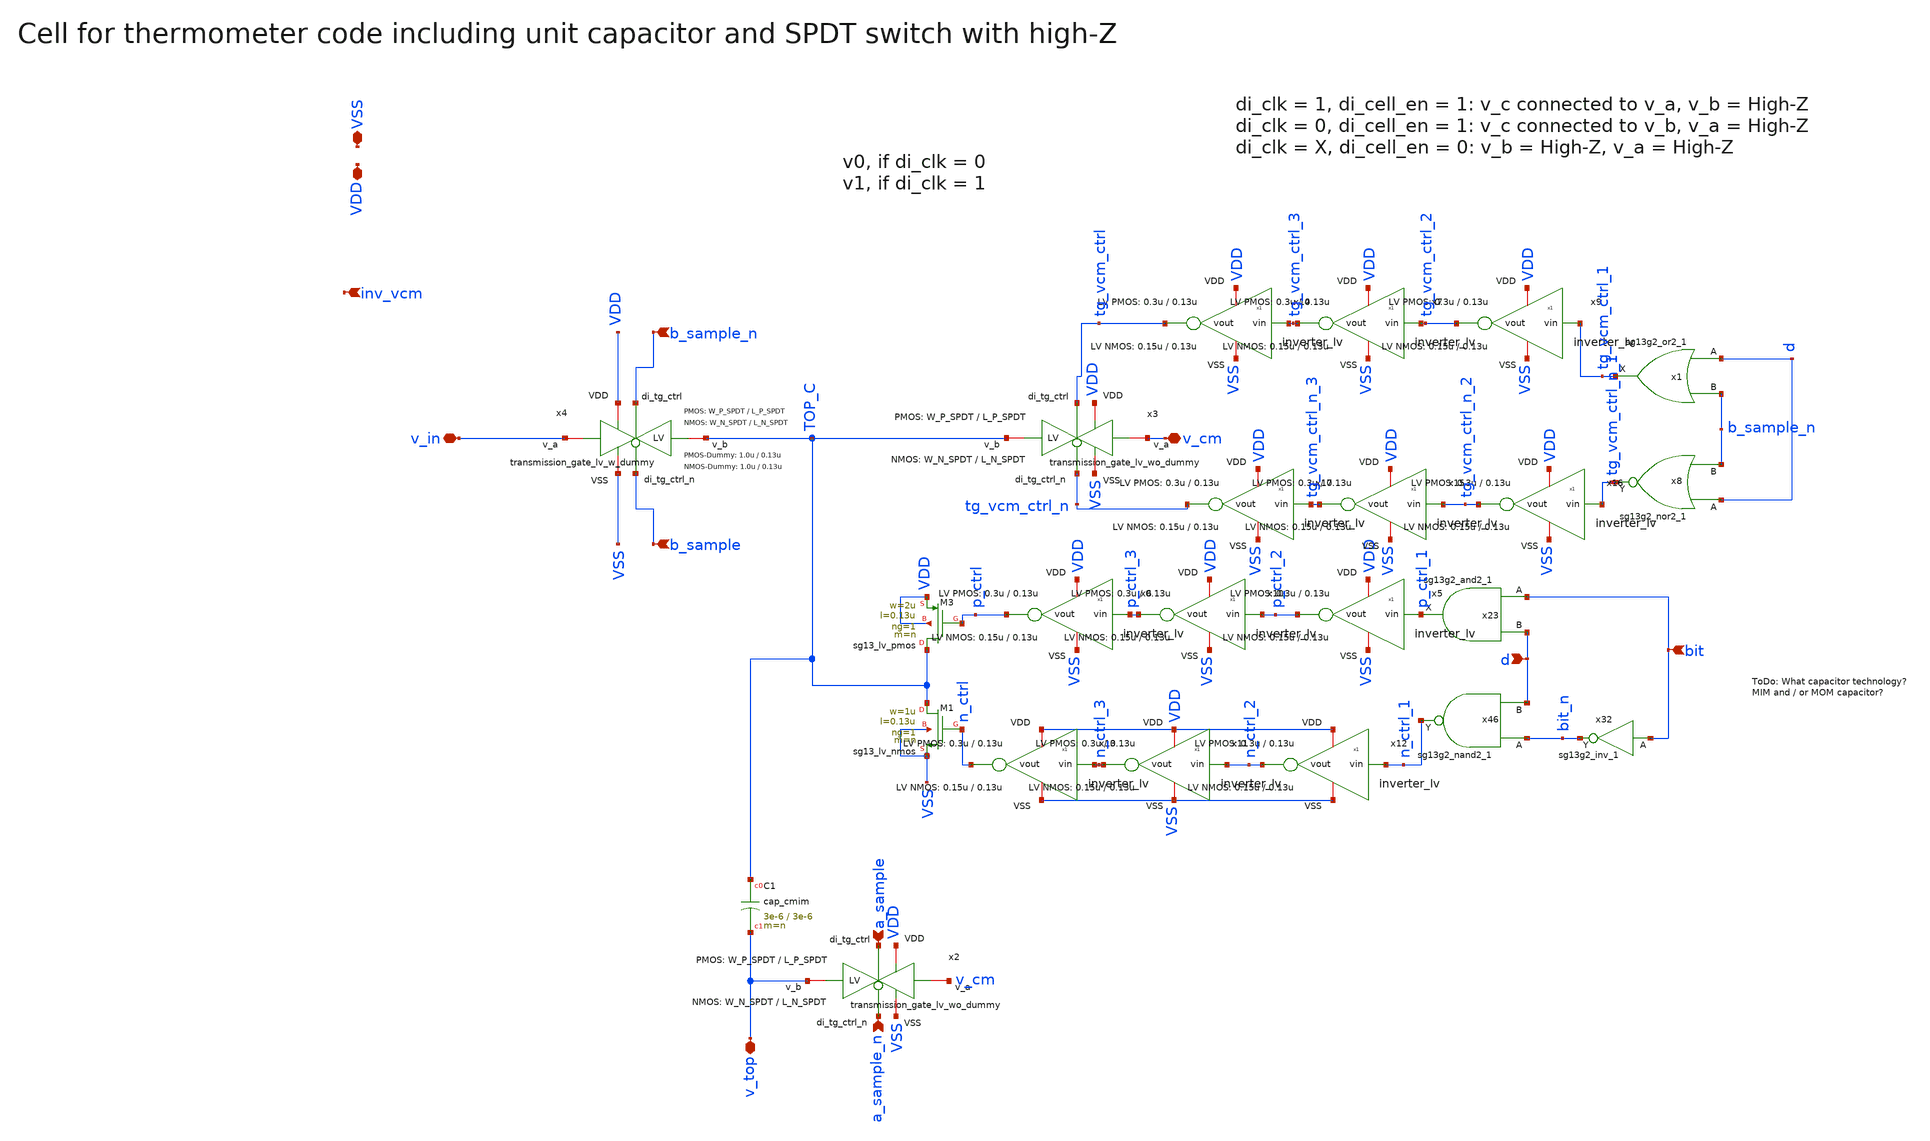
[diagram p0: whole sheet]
** sch_path: xschem/dac_icms_cell/unit_cell_n.sch
* IHP-GmbH/IHP-Open-PDK/ihp-sg13g2/libs.tech/xschem/sg13g2_stdcells/sg13g2_nor2_1.sch:
* Copyright 2023 IHP PDK Authors
* Licensed under the Apache License, Version 2.0 (the "License");
**.subckt unit_cell_n v_top a_sample a_sample_n b_sample b_sample_n v_in d v_cm bit inv_vcm VSS VDD
*.iopin v_top
*.ipin a_sample
*.ipin a_sample_n
*.ipin b_sample
*.ipin b_sample_n
*.iopin v_in
*.ipin d
*.iopin v_cm
*.ipin bit
*.ipin inv_vcm
*.iopin VSS
*.iopin VDD
x2 VDD a_sample VSS v_top v_cm a_sample_n transmission_gate_lv_wo_dummy W_P=W_P_SPDT L_P=L_P_SPDT
+ W_N=W_N_SPDT L_N=L_N_SPDT W_P_D=1.0u L_P_D=0.13u W_N_D=1.0u L_N_D=0.13u n=n
XC1 TOP_C v_top cap_cmim w=3e-6 l=3e-6 m=n mm_ok=1
XM1 TOP_C n_ctrl VSS VSS sg13_lv_nmos w=1u l=0.13u ng=1 m=n mm_ok=1
XM3 TOP_C p_ctrl VDD VDD sg13_lv_pmos w=2u l=0.13u ng=1 m=n mm_ok=1
x3 VDD tg_vcm_ctrl VSS TOP_C v_cm tg_vcm_ctrl_n transmission_gate_lv_wo_dummy W_P=W_P_SPDT
+ L_P=L_P_SPDT W_N=W_N_SPDT L_N=L_N_SPDT W_P_D=1.0u L_P_D=0.13u W_N_D=1.0u L_N_D=0.13u n=n
x4 VDD b_sample_n VSS TOP_C v_in b_sample transmission_gate_lv_w_dummy W_P=W_P_SPDT L_P=L_P_SPDT
+ W_N=W_N_SPDT L_N=L_N_SPDT W_P_D=1.0u L_P_D=0.13u W_N_D=1.0u L_N_D=0.13u n=n
x23 p_ctrl_1 bit d VDD VSS sg13g2_and2_1
x46 n_ctrl_1 bit_n d VDD VSS sg13g2_nand2_1
x32 bit_n bit VDD VSS sg13g2_inv_1
x1 tg_vcm_ctrl_1 d b_sample_n VDD VSS sg13g2_or2_1
x8 tg_vcm_ctrl_n_1 d b_sample_n VDD VSS sg13g2_nor2_1
x10 VDD p_ctrl_2 p_ctrl_3 VSS inverter_lv W_P=0.3u L_P=0.13u W_N=0.15u L_N=0.13u N_C=1
x5 VDD p_ctrl_1 p_ctrl_2 VSS inverter_lv W_P=0.3u L_P=0.13u W_N=0.15u L_N=0.13u N_C=1
x6 VDD p_ctrl_3 p_ctrl VSS inverter_lv W_P=0.3u L_P=0.13u W_N=0.15u L_N=0.13u N_C=1
x11 VDD n_ctrl_2 n_ctrl_3 VSS inverter_lv W_P=0.3u L_P=0.13u W_N=0.15u L_N=0.13u N_C=1
x12 VDD n_ctrl_1 n_ctrl_2 VSS inverter_lv W_P=0.3u L_P=0.13u W_N=0.15u L_N=0.13u N_C=1
x13 VDD n_ctrl_3 n_ctrl VSS inverter_lv W_P=0.3u L_P=0.13u W_N=0.15u L_N=0.13u N_C=1
x7 VDD tg_vcm_ctrl_2 tg_vcm_ctrl_3 VSS inverter_lv W_P=0.3u L_P=0.13u W_N=0.15u L_N=0.13u N_C=1
x9 VDD tg_vcm_ctrl_1 tg_vcm_ctrl_2 VSS inverter_lv W_P=0.3u L_P=0.13u W_N=0.15u L_N=0.13u N_C=1
x14 VDD tg_vcm_ctrl_3 tg_vcm_ctrl VSS inverter_lv W_P=0.3u L_P=0.13u W_N=0.15u L_N=0.13u N_C=1
x15 VDD tg_vcm_ctrl_n_2 tg_vcm_ctrl_n_3 VSS inverter_lv W_P=0.3u L_P=0.13u W_N=0.15u L_N=0.13u N_C=1
x16 VDD tg_vcm_ctrl_n_1 tg_vcm_ctrl_n_2 VSS inverter_lv W_P=0.3u L_P=0.13u W_N=0.15u L_N=0.13u N_C=1
x17 VDD tg_vcm_ctrl_n_3 tg_vcm_ctrl_n VSS inverter_lv W_P=0.3u L_P=0.13u W_N=0.15u L_N=0.13u N_C=1
**.ends

* expanding   symbol:  transmission_gate/transmission_gate_lv_wo_dummy.sym # of pins=6
** sym_path: xschem/transmission_gate/transmission_gate_lv_wo_dummy.sym
** sch_path: xschem/transmission_gate/transmission_gate_lv_wo_dummy.sch
.subckt transmission_gate_lv_wo_dummy VDD di_tg_ctrl VSS v_b v_a di_tg_ctrl_n  W_P=2.0u L_P=0.13u
+ W_N=2.0u L_N=0.13u W_P_D=1.0u L_P_D=0.13u W_N_D=1.0u L_N_D=0.13u n=1
*.iopin v_a
*.iopin v_b
*.iopin VDD
*.iopin VSS
*.ipin di_tg_ctrl
*.ipin di_tg_ctrl_n
XM1 v_a di_tg_ctrl v_b VSS sg13_lv_nmos w=W_N l=L_N ng=1 m=n mm_ok=1
XM2 v_a di_tg_ctrl_n v_b VDD sg13_lv_pmos w=W_P l=L_P ng=1 m=n mm_ok=1
.ends


* expanding   symbol:  transmission_gate/transmission_gate_lv_w_dummy.sym # of pins=6
** sym_path: xschem/transmission_gate/transmission_gate_lv_w_dummy.sym
** sch_path: xschem/transmission_gate/transmission_gate_lv_w_dummy.sch
.subckt transmission_gate_lv_w_dummy VDD di_tg_ctrl VSS v_b v_a di_tg_ctrl_n  W_P=2.0u L_P=0.13u
+ W_N=2.0u L_N=0.13u W_P_D=1.0u L_P_D=0.13u W_N_D=1.0u L_N_D=0.13u n=1
*.iopin v_a
*.iopin v_b
*.iopin VDD
*.iopin VSS
*.ipin di_tg_ctrl
*.ipin di_tg_ctrl_n
XM1 v_a di_tg_ctrl v_b VSS sg13_lv_nmos w=W_N l=L_N ng=1 m=n mm_ok=1
XM2 v_a di_tg_ctrl_n v_b VDD sg13_lv_pmos w=W_P l=L_P ng=1 m=n mm_ok=1
XMdummy2 v_b di_tg_ctrl v_b VDD sg13_lv_pmos w=W_P l=L_P ng=1 m={n/2} mm_ok=1
XMdummy1 v_b di_tg_ctrl_n v_b VSS sg13_lv_nmos w=W_N l=L_N ng=1 m={n/2} mm_ok=1
.ends


* expanding   symbol:  sg13g2_stdcells/sg13g2_and2_1.sym # of pins=3
** sym_path: sg13g2_stdcells/sg13g2_and2_1.sym
** sch_path: sg13g2_stdcells/sg13g2_and2_1.sch
.subckt sg13g2_and2_1 X A B VDD VSS
*.ipin A
*.ipin B
*.opin X
*.iopin VDD
*.iopin VSS
XM1 net1 A net2 VSS sg13_lv_nmos w=640.00n l=130.00n ng=1 m=1 mm_ok=1
XM2 net2 B VSS VSS sg13_lv_nmos w=640.00n l=130.00n ng=1 m=1 mm_ok=1
XM3 X net1 VSS VSS sg13_lv_nmos w=740.00n l=130.00n ng=1 m=1 mm_ok=1
XM4 net1 B VDD VDD sg13_lv_pmos w=840.00n l=130.00n ng=1 m=1 mm_ok=1
XM5 net1 A VDD VDD sg13_lv_pmos w=840.00n l=130.00n ng=1 m=1 mm_ok=1
XM6 X net1 VDD VDD sg13_lv_pmos w=1.12u l=130.00n ng=1 m=1 mm_ok=1
.ends


* expanding   symbol:  sg13g2_stdcells/sg13g2_nand2_1.sym # of pins=3
** sym_path: sg13g2_stdcells/sg13g2_nand2_1.sym
** sch_path: sg13g2_stdcells/sg13g2_nand2_1.sch
.subckt sg13g2_nand2_1 Y A B VDD VSS
*.iopin VDD
*.iopin VSS
*.ipin A
*.ipin B
*.opin Y
XM1 Y A net1 VSS sg13_lv_nmos w=740.00n l=130.00n ng=1 m=1 mm_ok=1
XM2 net1 B VSS VSS sg13_lv_nmos w=740.00n l=130.00n ng=1 m=1 mm_ok=1
XM3 Y A VDD VDD sg13_lv_pmos w=1.12u l=130.00n ng=1 m=1 mm_ok=1
XM4 Y B VDD VDD sg13_lv_pmos w=1.12u l=130.00n ng=1 m=1 mm_ok=1
.ends


* expanding   symbol:  sg13g2_stdcells/sg13g2_inv_1.sym # of pins=2
** sym_path: sg13g2_stdcells/sg13g2_inv_1.sym
** sch_path: sg13g2_stdcells/sg13g2_inv_1.sch
.subckt sg13g2_inv_1 Y A VDD VSS
*.opin Y
*.ipin A
*.iopin VDD
*.iopin VSS
XM1 Y A VSS VSS sg13_lv_nmos w=740.00n l=130.00n ng=1 m=1 mm_ok=1
XM2 Y A VDD VDD sg13_lv_pmos w=1.12u l=130.00n ng=1 m=1 mm_ok=1
.ends


* expanding   symbol:  sg13g2_stdcells/sg13g2_or2_1.sym # of pins=3
** sym_path: sg13g2_stdcells/sg13g2_or2_1.sym
** sch_path: sg13g2_stdcells/sg13g2_or2_1.sch
.subckt sg13g2_or2_1 X A B VDD VSS
*.opin X
*.ipin B
*.ipin A
*.iopin VDD
*.iopin VSS
XM1 net1 B VSS VSS sg13_lv_nmos w=550.00n l=130.00n ng=1 m=1 mm_ok=1
XM2 net1 A VSS VSS sg13_lv_nmos w=550.00n l=130.00n ng=1 m=1 mm_ok=1
XM3 X net1 VSS VSS sg13_lv_nmos w=740.00n l=130.00n ng=1 m=1 mm_ok=1
XM4 net2 A VDD VDD sg13_lv_pmos w=840.00n l=130.00n ng=1 m=1 mm_ok=1
XM5 net1 B net2 VDD sg13_lv_pmos w=840.00n l=130.00n ng=1 m=1 mm_ok=1
XM6 X net1 VDD VDD sg13_lv_pmos w=1.12u l=130.00n ng=1 m=1 mm_ok=1
.ends


* expanding   symbol:  sg13g2_stdcells/sg13g2_nor2_1.sym # of pins=3
** sym_path: sg13g2_stdcells/sg13g2_nor2_1.sym
** sch_path: sg13g2_stdcells/sg13g2_nor2_1.sch
.subckt sg13g2_nor2_1 Y A B VDD VSS
*.opin Y
*.ipin B
*.ipin A
*.iopin VDD
*.iopin VSS
XM1 Y A VSS VSS sg13_lv_nmos w=740.00n l=130.00n ng=1 m=1 mm_ok=1
XM2 Y B VSS VSS sg13_lv_nmos w=740.00n l=130.00n ng=1 m=1 mm_ok=1
XM3 net1 A VDD VDD sg13_lv_pmos w=1.12u l=130.00n ng=1 m=1 mm_ok=1
XM4 Y B net1 VDD sg13_lv_pmos w=1.12u l=130.00n ng=1 m=1 mm_ok=1
.ends


* expanding   symbol:  inverter/inverter_lv.sym # of pins=4
** sym_path: xschem/inverter/inverter_lv.sym
** sch_path: xschem/inverter/inverter_lv.sch
.subckt inverter_lv VDD vin vout VSS  W_P=3.0u L_P=0.13u W_N=1.0u L_N=0.13u N_C=1
*.ipin vin
*.iopin VDD
*.iopin VSS
*.opin vout
XM1 vout vin VDD VDD sg13_lv_pmos w=W_P l=L_P ng=1 m={N_C} mm_ok=1
XM2 vout vin VSS VSS sg13_lv_nmos w=W_N l=L_N ng=1 m={N_C} mm_ok=1
.ends

.end
